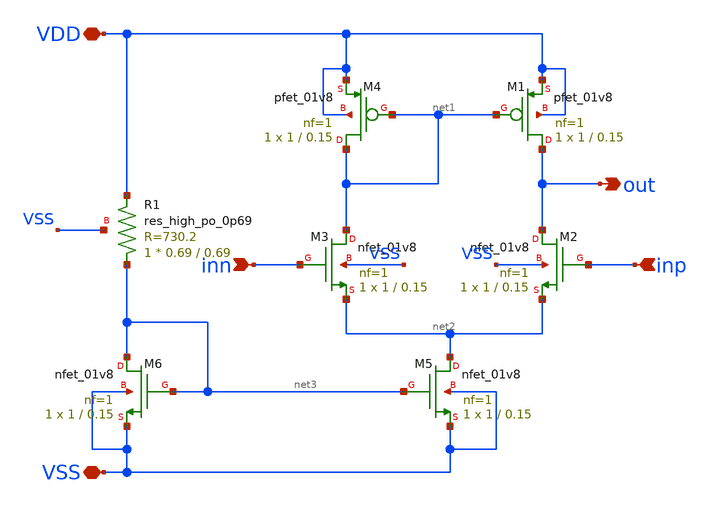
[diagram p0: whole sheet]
** sch_path: xschem/ota.sch
**.subckt ota VSS VDD inn out inp
*.iopin VSS
*.iopin VDD
*.ipin inn
*.opin out
*.ipin inp
XM3 net1 inn net2 VSS sky130_fd_pr__nfet_01v8 L=0.15 W=1 nf=1 ad='int((nf+1)/2) * W/nf * 0.29' as='int((nf+2)/2) * W/nf * 0.29'
+ pd='2*int((nf+1)/2) * (W/nf + 0.29)' ps='2*int((nf+2)/2) * (W/nf + 0.29)' nrd='0.29 / W' nrs='0.29 / W'
+ sa=0 sb=0 sd=0 mult=1 m=1
XM1 out net1 VDD VDD sky130_fd_pr__pfet_01v8 L=0.15 W=1 nf=1 ad='int((nf+1)/2) * W/nf * 0.29' as='int((nf+2)/2) * W/nf * 0.29'
+ pd='2*int((nf+1)/2) * (W/nf + 0.29)' ps='2*int((nf+2)/2) * (W/nf + 0.29)' nrd='0.29 / W' nrs='0.29 / W'
+ sa=0 sb=0 sd=0 mult=1 m=1
XM2 out inp net2 VSS sky130_fd_pr__nfet_01v8 L=0.15 W=1 nf=1 ad='int((nf+1)/2) * W/nf * 0.29' as='int((nf+2)/2) * W/nf * 0.29'
+ pd='2*int((nf+1)/2) * (W/nf + 0.29)' ps='2*int((nf+2)/2) * (W/nf + 0.29)' nrd='0.29 / W' nrs='0.29 / W'
+ sa=0 sb=0 sd=0 mult=1 m=1
XM4 net1 net1 VDD VDD sky130_fd_pr__pfet_01v8 L=0.15 W=1 nf=1 ad='int((nf+1)/2) * W/nf * 0.29' as='int((nf+2)/2) * W/nf * 0.29'
+ pd='2*int((nf+1)/2) * (W/nf + 0.29)' ps='2*int((nf+2)/2) * (W/nf + 0.29)' nrd='0.29 / W' nrs='0.29 / W'
+ sa=0 sb=0 sd=0 mult=1 m=1
XM5 net2 net3 VSS VSS sky130_fd_pr__nfet_01v8 L=0.15 W=1 nf=1 ad='int((nf+1)/2) * W/nf * 0.29' as='int((nf+2)/2) * W/nf * 0.29'
+ pd='2*int((nf+1)/2) * (W/nf + 0.29)' ps='2*int((nf+2)/2) * (W/nf + 0.29)' nrd='0.29 / W' nrs='0.29 / W'
+ sa=0 sb=0 sd=0 mult=1 m=1
XM6 net3 net3 VSS VSS sky130_fd_pr__nfet_01v8 L=0.15 W=1 nf=1 ad='int((nf+1)/2) * W/nf * 0.29' as='int((nf+2)/2) * W/nf * 0.29'
+ pd='2*int((nf+1)/2) * (W/nf + 0.29)' ps='2*int((nf+2)/2) * (W/nf + 0.29)' nrd='0.29 / W' nrs='0.29 / W'
+ sa=0 sb=0 sd=0 mult=1 m=1
XR1 net3 VDD VSS sky130_fd_pr__res_high_po_0p69 L=0.69 mult=1 m=1
**.ends
.end
